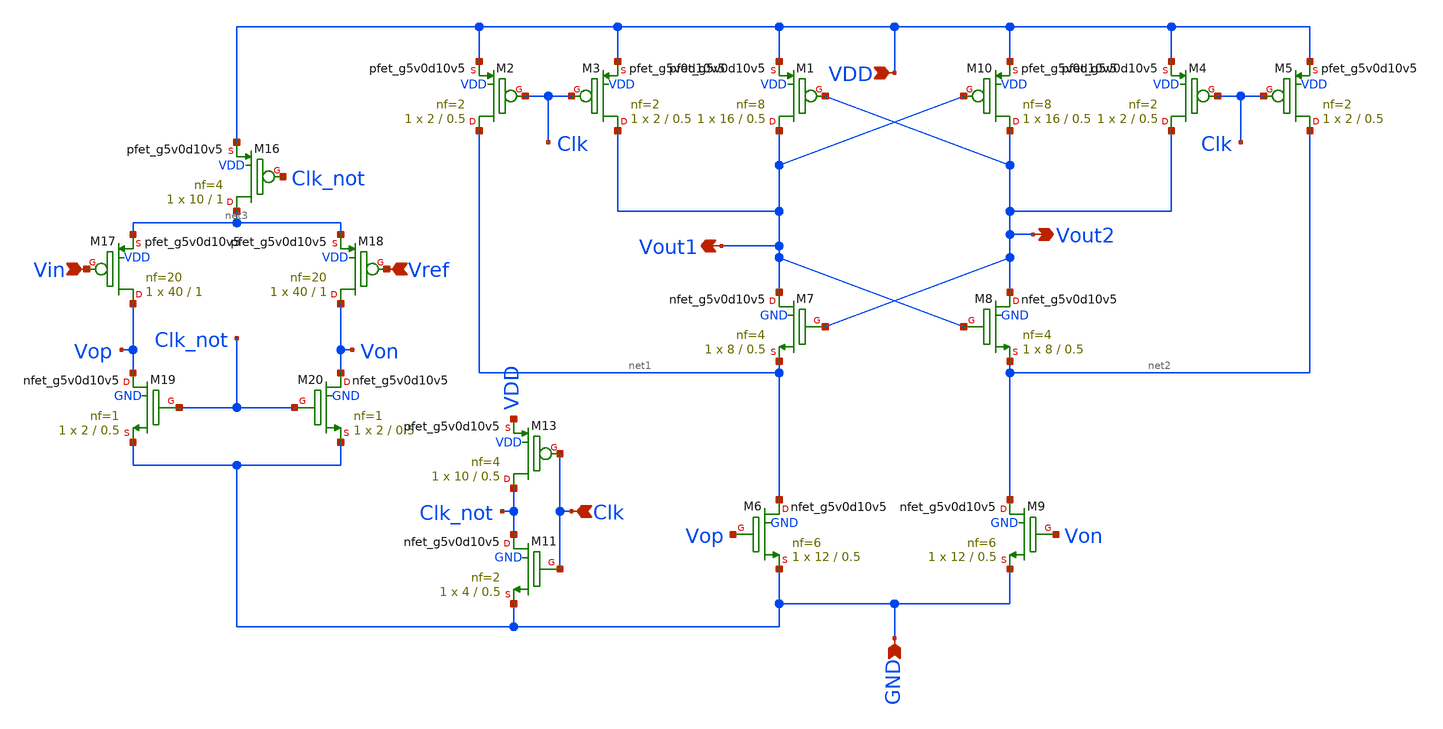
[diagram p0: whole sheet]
** sch_path: Strong_arm_latch.sch
**.subckt Strong_arm_latch Vin Vref Clk VDD Vout2 Vout1 GND
*.ipin Vin
*.ipin Vref
*.ipin Clk
*.ipin VDD
*.opin Vout2
*.opin Vout1
*.ipin GND
XM8 Vout2 Vout1 net2 GND sky130_fd_pr__nfet_g5v0d10v5 L=0.5 W=8 nf=4 ad='int((nf+1)/2) * W/nf * 0.29'
+ as='int((nf+2)/2) * W/nf * 0.29' pd='2*int((nf+1)/2) * (W/nf + 0.29)' ps='2*int((nf+2)/2) * (W/nf + 0.29)'
+ nrd='0.29 / W' nrs='0.29 / W' sa=0 sb=0 sd=0 mult=1 m=1
XM7 Vout1 Vout2 net1 GND sky130_fd_pr__nfet_g5v0d10v5 L=0.5 W=8 nf=4 ad='int((nf+1)/2) * W/nf * 0.29'
+ as='int((nf+2)/2) * W/nf * 0.29' pd='2*int((nf+1)/2) * (W/nf + 0.29)' ps='2*int((nf+2)/2) * (W/nf + 0.29)'
+ nrd='0.29 / W' nrs='0.29 / W' sa=0 sb=0 sd=0 mult=1 m=1
XM10 Vout2 Vout1 VDD VDD sky130_fd_pr__pfet_g5v0d10v5 L=0.5 W=16 nf=8 ad='int((nf+1)/2) * W/nf * 0.29'
+ as='int((nf+2)/2) * W/nf * 0.29' pd='2*int((nf+1)/2) * (W/nf + 0.29)' ps='2*int((nf+2)/2) * (W/nf + 0.29)'
+ nrd='0.29 / W' nrs='0.29 / W' sa=0 sb=0 sd=0 mult=1 m=1
XM1 Vout1 Vout2 VDD VDD sky130_fd_pr__pfet_g5v0d10v5 L=0.5 W=16 nf=8 ad='int((nf+1)/2) * W/nf * 0.29'
+ as='int((nf+2)/2) * W/nf * 0.29' pd='2*int((nf+1)/2) * (W/nf + 0.29)' ps='2*int((nf+2)/2) * (W/nf + 0.29)'
+ nrd='0.29 / W' nrs='0.29 / W' sa=0 sb=0 sd=0 mult=1 m=1
XM2 net1 Clk VDD VDD sky130_fd_pr__pfet_g5v0d10v5 L=0.5 W=2 nf=2 ad='int((nf+1)/2) * W/nf * 0.29' as='int((nf+2)/2) * W/nf * 0.29'
+ pd='2*int((nf+1)/2) * (W/nf + 0.29)' ps='2*int((nf+2)/2) * (W/nf + 0.29)' nrd='0.29 / W' nrs='0.29 / W'
+ sa=0 sb=0 sd=0 mult=1 m=1
XM3 Vout1 Clk VDD VDD sky130_fd_pr__pfet_g5v0d10v5 L=0.5 W=2 nf=2 ad='int((nf+1)/2) * W/nf * 0.29' as='int((nf+2)/2) * W/nf * 0.29'
+ pd='2*int((nf+1)/2) * (W/nf + 0.29)' ps='2*int((nf+2)/2) * (W/nf + 0.29)' nrd='0.29 / W' nrs='0.29 / W'
+ sa=0 sb=0 sd=0 mult=1 m=1
XM4 Vout2 Clk VDD VDD sky130_fd_pr__pfet_g5v0d10v5 L=0.5 W=2 nf=2 ad='int((nf+1)/2) * W/nf * 0.29' as='int((nf+2)/2) * W/nf * 0.29'
+ pd='2*int((nf+1)/2) * (W/nf + 0.29)' ps='2*int((nf+2)/2) * (W/nf + 0.29)' nrd='0.29 / W' nrs='0.29 / W'
+ sa=0 sb=0 sd=0 mult=1 m=1
XM5 net2 Clk VDD VDD sky130_fd_pr__pfet_g5v0d10v5 L=0.5 W=2 nf=2 ad='int((nf+1)/2) * W/nf * 0.29' as='int((nf+2)/2) * W/nf * 0.29'
+ pd='2*int((nf+1)/2) * (W/nf + 0.29)' ps='2*int((nf+2)/2) * (W/nf + 0.29)' nrd='0.29 / W' nrs='0.29 / W'
+ sa=0 sb=0 sd=0 mult=1 m=1
XM6 net1 Vop GND GND sky130_fd_pr__nfet_g5v0d10v5 L=0.5 W=12 nf=6 ad='int((nf+1)/2) * W/nf * 0.29' as='int((nf+2)/2) * W/nf * 0.29'
+ pd='2*int((nf+1)/2) * (W/nf + 0.29)' ps='2*int((nf+2)/2) * (W/nf + 0.29)' nrd='0.29 / W' nrs='0.29 / W'
+ sa=0 sb=0 sd=0 mult=1 m=1
XM9 net2 Von GND GND sky130_fd_pr__nfet_g5v0d10v5 L=0.5 W=12 nf=6 ad='int((nf+1)/2) * W/nf * 0.29' as='int((nf+2)/2) * W/nf * 0.29'
+ pd='2*int((nf+1)/2) * (W/nf + 0.29)' ps='2*int((nf+2)/2) * (W/nf + 0.29)' nrd='0.29 / W' nrs='0.29 / W'
+ sa=0 sb=0 sd=0 mult=1 m=1
XM16 net3 Clk_not VDD VDD sky130_fd_pr__pfet_g5v0d10v5 L=1 W=10 nf=4 ad='int((nf+1)/2) * W/nf * 0.29'
+ as='int((nf+2)/2) * W/nf * 0.29' pd='2*int((nf+1)/2) * (W/nf + 0.29)' ps='2*int((nf+2)/2) * (W/nf + 0.29)'
+ nrd='0.29 / W' nrs='0.29 / W' sa=0 sb=0 sd=0 mult=1 m=1
XM17 Vop Vin net3 VDD sky130_fd_pr__pfet_g5v0d10v5 L=1 W=40 nf=20 ad='int((nf+1)/2) * W/nf * 0.29' as='int((nf+2)/2) * W/nf * 0.29'
+ pd='2*int((nf+1)/2) * (W/nf + 0.29)' ps='2*int((nf+2)/2) * (W/nf + 0.29)' nrd='0.29 / W' nrs='0.29 / W'
+ sa=0 sb=0 sd=0 mult=1 m=1
XM18 Von Vref net3 VDD sky130_fd_pr__pfet_g5v0d10v5 L=1 W=40 nf=20 ad='int((nf+1)/2) * W/nf * 0.29' as='int((nf+2)/2) * W/nf * 0.29'
+ pd='2*int((nf+1)/2) * (W/nf + 0.29)' ps='2*int((nf+2)/2) * (W/nf + 0.29)' nrd='0.29 / W' nrs='0.29 / W'
+ sa=0 sb=0 sd=0 mult=1 m=1
XM19 Vop Clk_not GND GND sky130_fd_pr__nfet_g5v0d10v5 L=0.5 W=2 nf=1 ad='int((nf+1)/2) * W/nf * 0.29'
+ as='int((nf+2)/2) * W/nf * 0.29' pd='2*int((nf+1)/2) * (W/nf + 0.29)' ps='2*int((nf+2)/2) * (W/nf + 0.29)'
+ nrd='0.29 / W' nrs='0.29 / W' sa=0 sb=0 sd=0 mult=1 m=1
XM20 Von Clk_not GND GND sky130_fd_pr__nfet_g5v0d10v5 L=0.5 W=2 nf=1 ad='int((nf+1)/2) * W/nf * 0.29'
+ as='int((nf+2)/2) * W/nf * 0.29' pd='2*int((nf+1)/2) * (W/nf + 0.29)' ps='2*int((nf+2)/2) * (W/nf + 0.29)'
+ nrd='0.29 / W' nrs='0.29 / W' sa=0 sb=0 sd=0 mult=1 m=1
XM11 Clk_not Clk GND GND sky130_fd_pr__nfet_g5v0d10v5 L=0.5 W=4 nf=2 ad='int((nf+1)/2) * W/nf * 0.29'
+ as='int((nf+2)/2) * W/nf * 0.29' pd='2*int((nf+1)/2) * (W/nf + 0.29)' ps='2*int((nf+2)/2) * (W/nf + 0.29)'
+ nrd='0.29 / W' nrs='0.29 / W' sa=0 sb=0 sd=0 mult=1 m=1
XM13 Clk_not Clk VDD VDD sky130_fd_pr__pfet_g5v0d10v5 L=0.5 W=10 nf=4 ad='int((nf+1)/2) * W/nf * 0.29'
+ as='int((nf+2)/2) * W/nf * 0.29' pd='2*int((nf+1)/2) * (W/nf + 0.29)' ps='2*int((nf+2)/2) * (W/nf + 0.29)'
+ nrd='0.29 / W' nrs='0.29 / W' sa=0 sb=0 sd=0 mult=1 m=1
**.ends
.end
